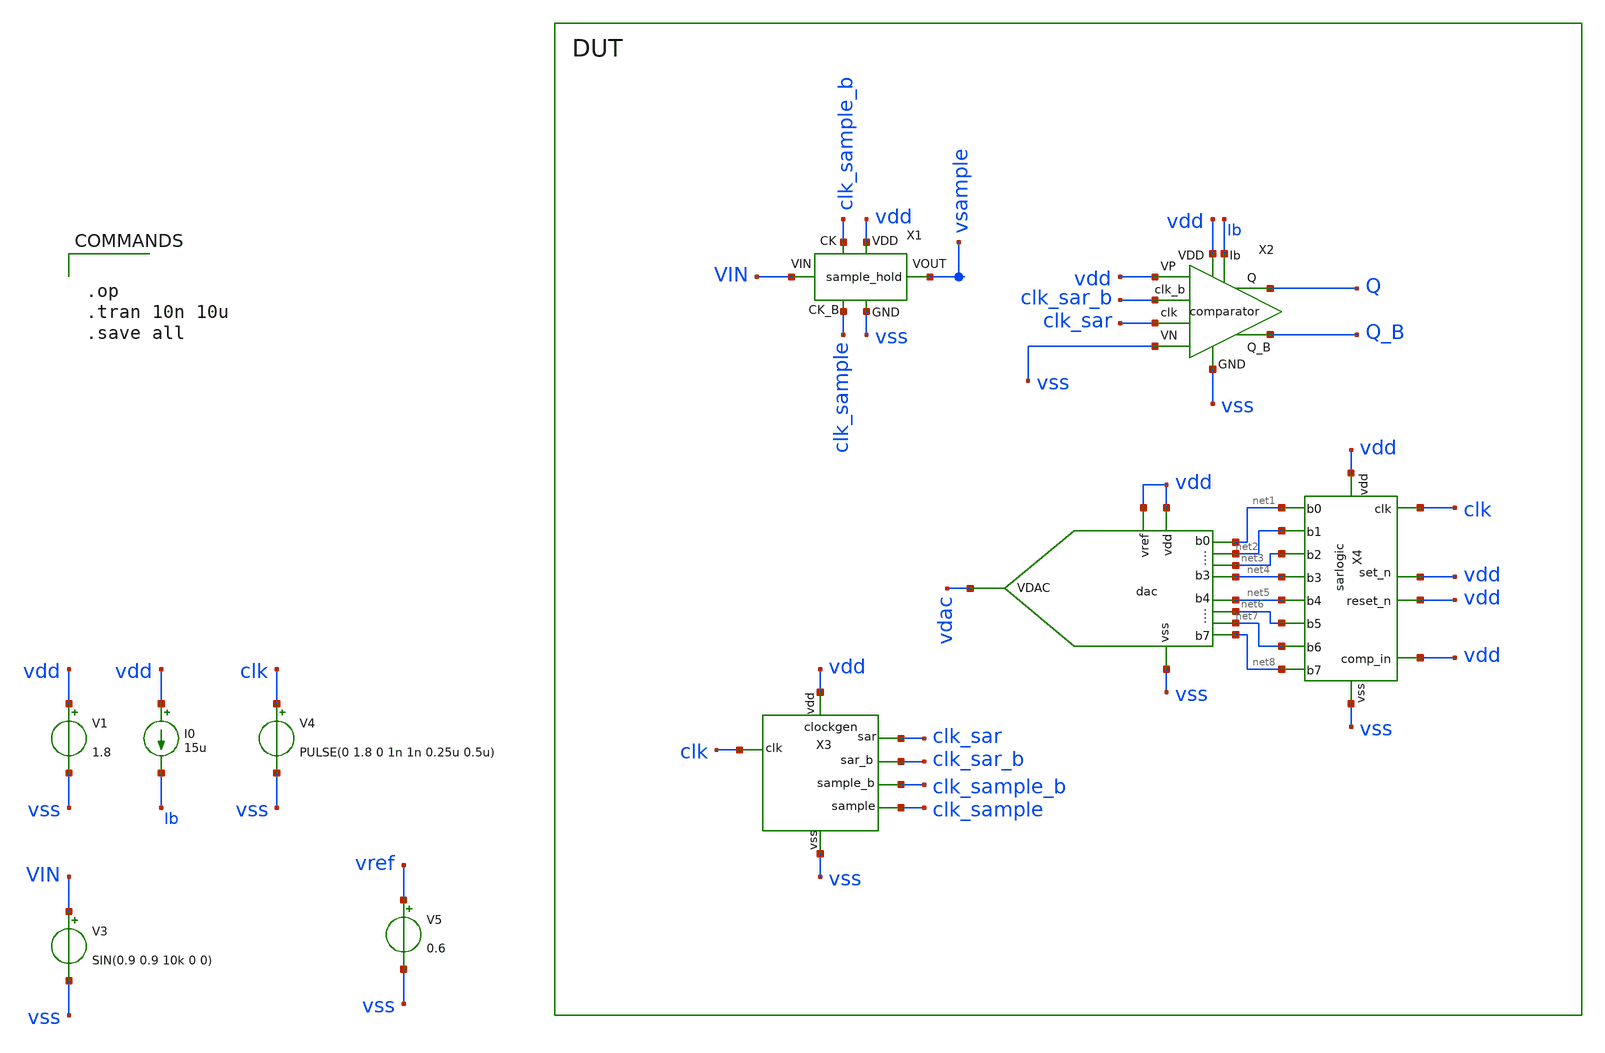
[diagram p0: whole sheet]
** sch_path: xschem/adc_top.sch
.lib $::SKYWATER_MODELS/sky130.lib.spice tt
.include $::SKYWATER_STDCELLS/sky130_fd_sc_hd.spice

**.subckt adc_top
V1 vdd vss 1.8
V3 VIN vss SIN(0.9 0.9 10k 0 0)
V4 clk vss PULSE(0 1.8 0 1n 1n 0.25u 0.5u)
I0 vdd Ib 15u
X2 vdd vss vss Q_B Q vdd clk_sar Ib clk_sar_b comparator
X1 vss vdd VIN vsample clk_sample_b clk_sample sample_hold
X3 clk vdd clk_sar clk_sample vss clk_sar_b clk_sample_b clockgen
X4 net1 net2 clk vdd vdd vdd vdd vss net3 net4 net5 net6 net7 net8 sarlogic
X1 vss vdac vdd vdd net1 net2 net3 net4 net5 net6 net7 net8 dac
V5 vref vss 0.6
**** begin user architecture code


.op
.tran 10n 10u
.save all


**** end user architecture code
**.ends
.end
